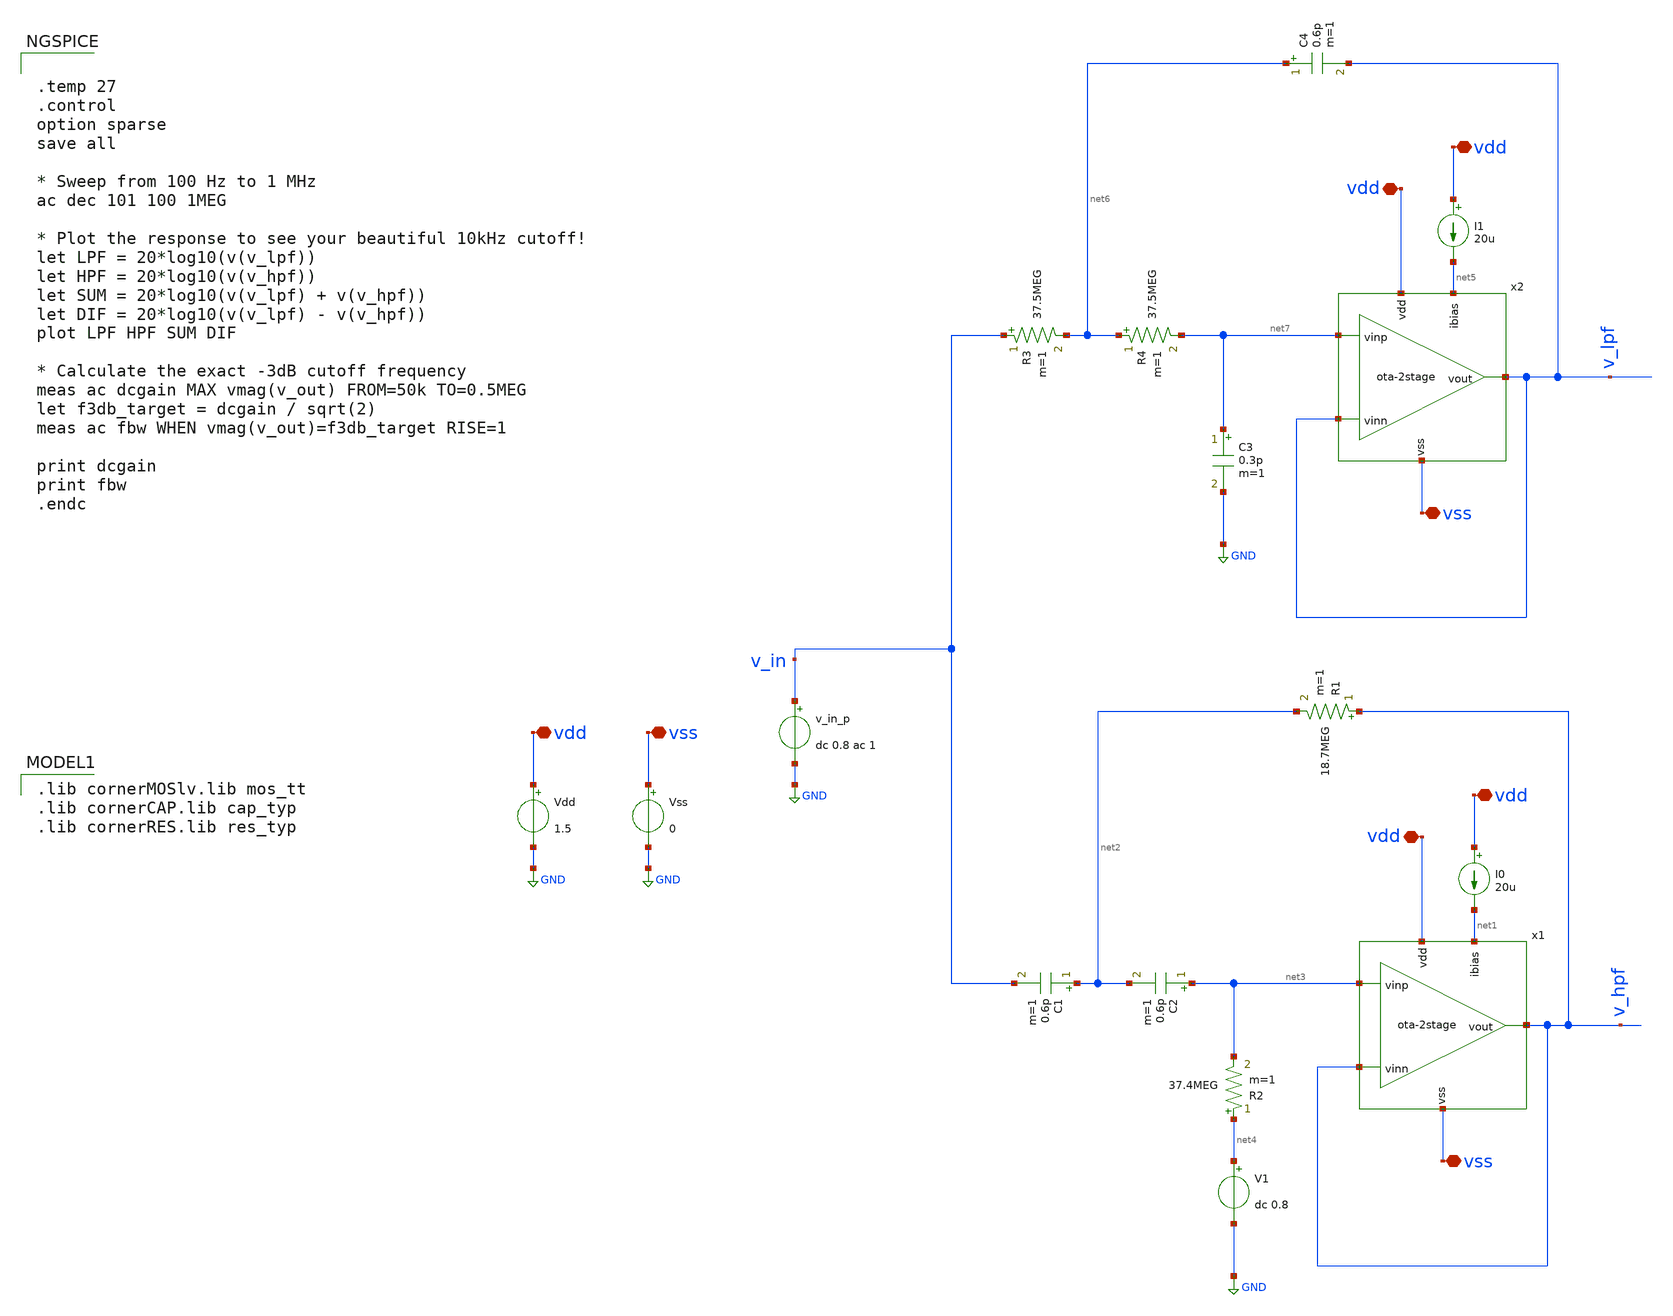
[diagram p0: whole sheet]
** sch_path: testbench/ota-2stage_tb-sk-LR2.sch
**.subckt ota-2stage_tb-sk-LR2 vdd vdd vdd vss vss vdd vdd vss
*.iopin vdd
*.iopin vdd
*.iopin vdd
*.iopin vss
*.iopin vss
*.iopin vdd
*.iopin vdd
*.iopin vss
I0 vdd net1 20u
Vdd vdd GND 1.5
Vss vss GND 0
v_in_p v_in GND dc 0.8 ac 1
x1 vdd net1 v_hpf v_hpf net3 vss ota-2stage
R1 v_hpf net2 18.7MEG m=1
R2 net4 net3 37.4MEG m=1
C1 net2 v_in 0.6p m=1
C2 net3 net2 0.6p m=1
V1 net4 GND dc 0.8
I1 vdd net5 20u
R3 v_in net6 37.5MEG m=1
R4 net6 net7 37.5MEG m=1
C3 net7 GND 0.3p m=1
C4 net6 v_lpf 0.6p m=1
x2 vdd net5 v_lpf v_lpf net7 vss ota-2stage
**** begin user architecture code


.temp 27
.control
option sparse
save all

* Sweep from 100 Hz to 1 MHz
ac dec 101 100 1MEG

* Plot the response to see your beautiful 10kHz cutoff!
let LPF = 20*log10(v(v_lpf))
let HPF = 20*log10(v(v_hpf))
let SUM = 20*log10(v(v_lpf) + v(v_hpf))
let DIF = 20*log10(v(v_lpf) - v(v_hpf))
plot LPF HPF SUM DIF

* Calculate the exact -3dB cutoff frequency
meas ac dcgain MAX vmag(v_out) FROM=50k TO=0.5MEG
let f3db_target = dcgain / sqrt(2)
meas ac fbw WHEN vmag(v_out)=f3db_target RISE=1

print dcgain
print fbw
.endc


 .lib cornerMOSlv.lib mos_tt
.lib cornerCAP.lib cap_typ
.lib cornerRES.lib res_typ

**** end user architecture code
**.ends
.GLOBAL GND
.end
